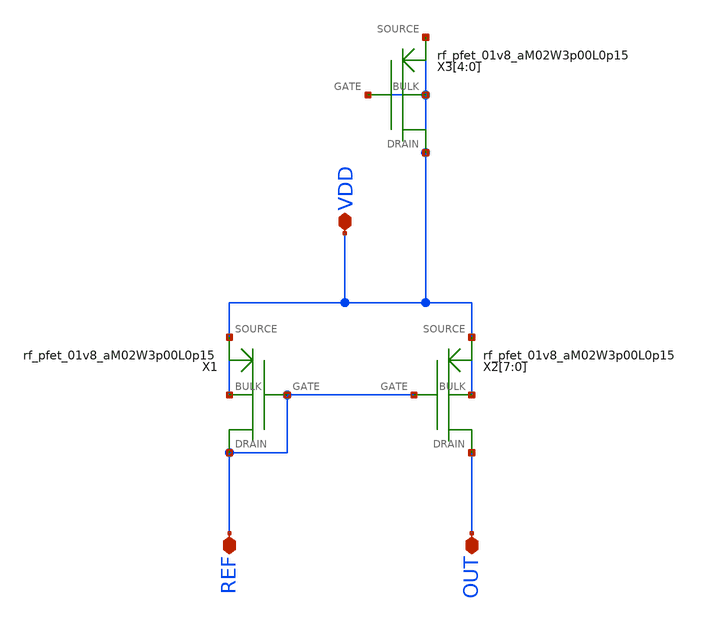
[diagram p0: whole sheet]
** sch_path: xschem/vco/parts/vco_pmirr.sch
**.subckt vco_pmirr OUT REF VDD
*.iopin OUT
*.iopin REF
*.iopin VDD
X1 VDD REF REF VDD rf_pfet_01v8_aM02W3p00L0p15
X2[7] VDD REF OUT VDD rf_pfet_01v8_aM02W3p00L0p15
X2[6] VDD REF OUT VDD rf_pfet_01v8_aM02W3p00L0p15
X2[5] VDD REF OUT VDD rf_pfet_01v8_aM02W3p00L0p15
X2[4] VDD REF OUT VDD rf_pfet_01v8_aM02W3p00L0p15
X2[3] VDD REF OUT VDD rf_pfet_01v8_aM02W3p00L0p15
X2[2] VDD REF OUT VDD rf_pfet_01v8_aM02W3p00L0p15
X2[1] VDD REF OUT VDD rf_pfet_01v8_aM02W3p00L0p15
X2[0] VDD REF OUT VDD rf_pfet_01v8_aM02W3p00L0p15
X3[4] VDD VDD VDD VDD rf_pfet_01v8_aM02W3p00L0p15
X3[3] VDD VDD VDD VDD rf_pfet_01v8_aM02W3p00L0p15
X3[2] VDD VDD VDD VDD rf_pfet_01v8_aM02W3p00L0p15
X3[1] VDD VDD VDD VDD rf_pfet_01v8_aM02W3p00L0p15
X3[0] VDD VDD VDD VDD rf_pfet_01v8_aM02W3p00L0p15
**.ends
.end
